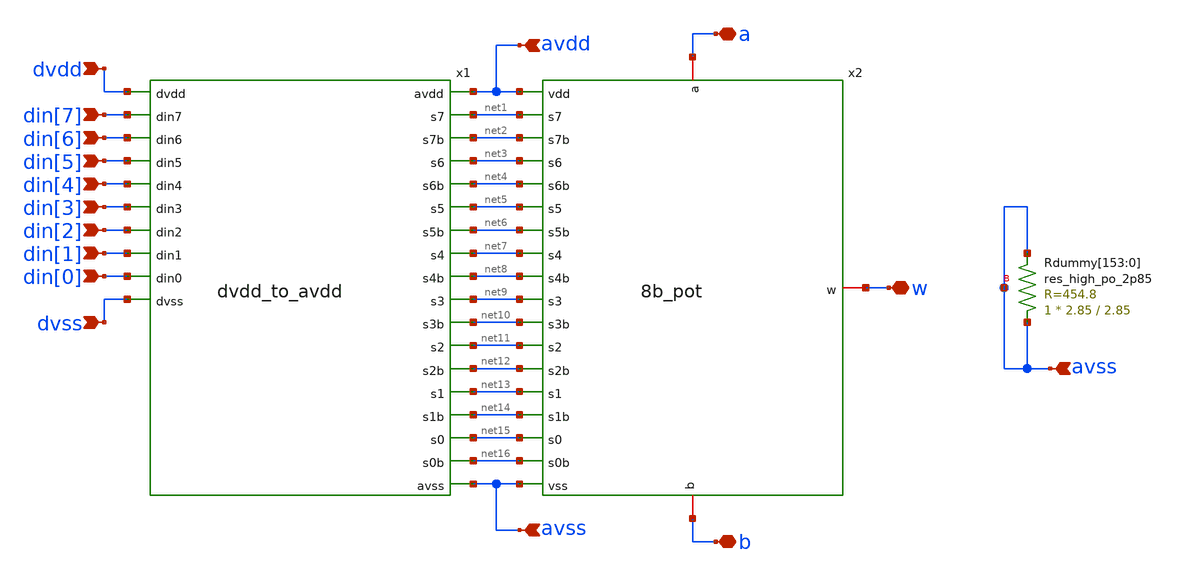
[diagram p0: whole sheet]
** sch_path: xschem/sky130_di_ip__rheostat_8bit.sch
**.subckt sky130_di_ip__rheostat_8bit avdd dvdd dvss avss b w a din[0] din[1] din[2] din[3] din[4]
*+ din[5] din[6] din[7] avss
*.ipin avdd
*.ipin dvdd
*.ipin dvss
*.ipin avss
*.iopin b
*.iopin w
*.iopin a
*.ipin din[0]
*.ipin din[1]
*.ipin din[2]
*.ipin din[3]
*.ipin din[4]
*.ipin din[5]
*.ipin din[6]
*.ipin din[7]
*.ipin avss
x1 avdd dvdd net1 din[7] net2 net3 din[6] net4 net5 din[5] net6 net7 din[4] net8 net9 din[3] net10
+ net11 din[2] net12 net13 din[1] net14 net15 din[0] net16 dvss avss dvdd_to_avdd
x2 avdd a net1 net2 net3 net4 net5 net6 net7 net8 w net9 net10 net11 net12 net13 net14 net15 net16 b
+ avss 8b_pot
XRdummy[153] avss avss avss sky130_fd_pr__res_high_po_2p85 L=2.85 mult=1 m=1
XRdummy[152] avss avss avss sky130_fd_pr__res_high_po_2p85 L=2.85 mult=1 m=1
XRdummy[151] avss avss avss sky130_fd_pr__res_high_po_2p85 L=2.85 mult=1 m=1
XRdummy[150] avss avss avss sky130_fd_pr__res_high_po_2p85 L=2.85 mult=1 m=1
XRdummy[149] avss avss avss sky130_fd_pr__res_high_po_2p85 L=2.85 mult=1 m=1
XRdummy[148] avss avss avss sky130_fd_pr__res_high_po_2p85 L=2.85 mult=1 m=1
XRdummy[147] avss avss avss sky130_fd_pr__res_high_po_2p85 L=2.85 mult=1 m=1
XRdummy[146] avss avss avss sky130_fd_pr__res_high_po_2p85 L=2.85 mult=1 m=1
XRdummy[145] avss avss avss sky130_fd_pr__res_high_po_2p85 L=2.85 mult=1 m=1
XRdummy[144] avss avss avss sky130_fd_pr__res_high_po_2p85 L=2.85 mult=1 m=1
XRdummy[143] avss avss avss sky130_fd_pr__res_high_po_2p85 L=2.85 mult=1 m=1
XRdummy[142] avss avss avss sky130_fd_pr__res_high_po_2p85 L=2.85 mult=1 m=1
XRdummy[141] avss avss avss sky130_fd_pr__res_high_po_2p85 L=2.85 mult=1 m=1
XRdummy[140] avss avss avss sky130_fd_pr__res_high_po_2p85 L=2.85 mult=1 m=1
XRdummy[139] avss avss avss sky130_fd_pr__res_high_po_2p85 L=2.85 mult=1 m=1
XRdummy[138] avss avss avss sky130_fd_pr__res_high_po_2p85 L=2.85 mult=1 m=1
XRdummy[137] avss avss avss sky130_fd_pr__res_high_po_2p85 L=2.85 mult=1 m=1
XRdummy[136] avss avss avss sky130_fd_pr__res_high_po_2p85 L=2.85 mult=1 m=1
XRdummy[135] avss avss avss sky130_fd_pr__res_high_po_2p85 L=2.85 mult=1 m=1
XRdummy[134] avss avss avss sky130_fd_pr__res_high_po_2p85 L=2.85 mult=1 m=1
XRdummy[133] avss avss avss sky130_fd_pr__res_high_po_2p85 L=2.85 mult=1 m=1
XRdummy[132] avss avss avss sky130_fd_pr__res_high_po_2p85 L=2.85 mult=1 m=1
XRdummy[131] avss avss avss sky130_fd_pr__res_high_po_2p85 L=2.85 mult=1 m=1
XRdummy[130] avss avss avss sky130_fd_pr__res_high_po_2p85 L=2.85 mult=1 m=1
XRdummy[129] avss avss avss sky130_fd_pr__res_high_po_2p85 L=2.85 mult=1 m=1
XRdummy[128] avss avss avss sky130_fd_pr__res_high_po_2p85 L=2.85 mult=1 m=1
XRdummy[127] avss avss avss sky130_fd_pr__res_high_po_2p85 L=2.85 mult=1 m=1
XRdummy[126] avss avss avss sky130_fd_pr__res_high_po_2p85 L=2.85 mult=1 m=1
XRdummy[125] avss avss avss sky130_fd_pr__res_high_po_2p85 L=2.85 mult=1 m=1
XRdummy[124] avss avss avss sky130_fd_pr__res_high_po_2p85 L=2.85 mult=1 m=1
XRdummy[123] avss avss avss sky130_fd_pr__res_high_po_2p85 L=2.85 mult=1 m=1
XRdummy[122] avss avss avss sky130_fd_pr__res_high_po_2p85 L=2.85 mult=1 m=1
XRdummy[121] avss avss avss sky130_fd_pr__res_high_po_2p85 L=2.85 mult=1 m=1
XRdummy[120] avss avss avss sky130_fd_pr__res_high_po_2p85 L=2.85 mult=1 m=1
XRdummy[119] avss avss avss sky130_fd_pr__res_high_po_2p85 L=2.85 mult=1 m=1
XRdummy[118] avss avss avss sky130_fd_pr__res_high_po_2p85 L=2.85 mult=1 m=1
XRdummy[117] avss avss avss sky130_fd_pr__res_high_po_2p85 L=2.85 mult=1 m=1
XRdummy[116] avss avss avss sky130_fd_pr__res_high_po_2p85 L=2.85 mult=1 m=1
XRdummy[115] avss avss avss sky130_fd_pr__res_high_po_2p85 L=2.85 mult=1 m=1
XRdummy[114] avss avss avss sky130_fd_pr__res_high_po_2p85 L=2.85 mult=1 m=1
XRdummy[113] avss avss avss sky130_fd_pr__res_high_po_2p85 L=2.85 mult=1 m=1
XRdummy[112] avss avss avss sky130_fd_pr__res_high_po_2p85 L=2.85 mult=1 m=1
XRdummy[111] avss avss avss sky130_fd_pr__res_high_po_2p85 L=2.85 mult=1 m=1
XRdummy[110] avss avss avss sky130_fd_pr__res_high_po_2p85 L=2.85 mult=1 m=1
XRdummy[109] avss avss avss sky130_fd_pr__res_high_po_2p85 L=2.85 mult=1 m=1
XRdummy[108] avss avss avss sky130_fd_pr__res_high_po_2p85 L=2.85 mult=1 m=1
XRdummy[107] avss avss avss sky130_fd_pr__res_high_po_2p85 L=2.85 mult=1 m=1
XRdummy[106] avss avss avss sky130_fd_pr__res_high_po_2p85 L=2.85 mult=1 m=1
XRdummy[105] avss avss avss sky130_fd_pr__res_high_po_2p85 L=2.85 mult=1 m=1
XRdummy[104] avss avss avss sky130_fd_pr__res_high_po_2p85 L=2.85 mult=1 m=1
XRdummy[103] avss avss avss sky130_fd_pr__res_high_po_2p85 L=2.85 mult=1 m=1
XRdummy[102] avss avss avss sky130_fd_pr__res_high_po_2p85 L=2.85 mult=1 m=1
XRdummy[101] avss avss avss sky130_fd_pr__res_high_po_2p85 L=2.85 mult=1 m=1
XRdummy[100] avss avss avss sky130_fd_pr__res_high_po_2p85 L=2.85 mult=1 m=1
XRdummy[99] avss avss avss sky130_fd_pr__res_high_po_2p85 L=2.85 mult=1 m=1
XRdummy[98] avss avss avss sky130_fd_pr__res_high_po_2p85 L=2.85 mult=1 m=1
XRdummy[97] avss avss avss sky130_fd_pr__res_high_po_2p85 L=2.85 mult=1 m=1
XRdummy[96] avss avss avss sky130_fd_pr__res_high_po_2p85 L=2.85 mult=1 m=1
XRdummy[95] avss avss avss sky130_fd_pr__res_high_po_2p85 L=2.85 mult=1 m=1
XRdummy[94] avss avss avss sky130_fd_pr__res_high_po_2p85 L=2.85 mult=1 m=1
XRdummy[93] avss avss avss sky130_fd_pr__res_high_po_2p85 L=2.85 mult=1 m=1
XRdummy[92] avss avss avss sky130_fd_pr__res_high_po_2p85 L=2.85 mult=1 m=1
XRdummy[91] avss avss avss sky130_fd_pr__res_high_po_2p85 L=2.85 mult=1 m=1
XRdummy[90] avss avss avss sky130_fd_pr__res_high_po_2p85 L=2.85 mult=1 m=1
XRdummy[89] avss avss avss sky130_fd_pr__res_high_po_2p85 L=2.85 mult=1 m=1
XRdummy[88] avss avss avss sky130_fd_pr__res_high_po_2p85 L=2.85 mult=1 m=1
XRdummy[87] avss avss avss sky130_fd_pr__res_high_po_2p85 L=2.85 mult=1 m=1
XRdummy[86] avss avss avss sky130_fd_pr__res_high_po_2p85 L=2.85 mult=1 m=1
XRdummy[85] avss avss avss sky130_fd_pr__res_high_po_2p85 L=2.85 mult=1 m=1
XRdummy[84] avss avss avss sky130_fd_pr__res_high_po_2p85 L=2.85 mult=1 m=1
XRdummy[83] avss avss avss sky130_fd_pr__res_high_po_2p85 L=2.85 mult=1 m=1
XRdummy[82] avss avss avss sky130_fd_pr__res_high_po_2p85 L=2.85 mult=1 m=1
XRdummy[81] avss avss avss sky130_fd_pr__res_high_po_2p85 L=2.85 mult=1 m=1
XRdummy[80] avss avss avss sky130_fd_pr__res_high_po_2p85 L=2.85 mult=1 m=1
XRdummy[79] avss avss avss sky130_fd_pr__res_high_po_2p85 L=2.85 mult=1 m=1
XRdummy[78] avss avss avss sky130_fd_pr__res_high_po_2p85 L=2.85 mult=1 m=1
XRdummy[77] avss avss avss sky130_fd_pr__res_high_po_2p85 L=2.85 mult=1 m=1
XRdummy[76] avss avss avss sky130_fd_pr__res_high_po_2p85 L=2.85 mult=1 m=1
XRdummy[75] avss avss avss sky130_fd_pr__res_high_po_2p85 L=2.85 mult=1 m=1
XRdummy[74] avss avss avss sky130_fd_pr__res_high_po_2p85 L=2.85 mult=1 m=1
XRdummy[73] avss avss avss sky130_fd_pr__res_high_po_2p85 L=2.85 mult=1 m=1
XRdummy[72] avss avss avss sky130_fd_pr__res_high_po_2p85 L=2.85 mult=1 m=1
XRdummy[71] avss avss avss sky130_fd_pr__res_high_po_2p85 L=2.85 mult=1 m=1
XRdummy[70] avss avss avss sky130_fd_pr__res_high_po_2p85 L=2.85 mult=1 m=1
XRdummy[69] avss avss avss sky130_fd_pr__res_high_po_2p85 L=2.85 mult=1 m=1
XRdummy[68] avss avss avss sky130_fd_pr__res_high_po_2p85 L=2.85 mult=1 m=1
XRdummy[67] avss avss avss sky130_fd_pr__res_high_po_2p85 L=2.85 mult=1 m=1
XRdummy[66] avss avss avss sky130_fd_pr__res_high_po_2p85 L=2.85 mult=1 m=1
XRdummy[65] avss avss avss sky130_fd_pr__res_high_po_2p85 L=2.85 mult=1 m=1
XRdummy[64] avss avss avss sky130_fd_pr__res_high_po_2p85 L=2.85 mult=1 m=1
XRdummy[63] avss avss avss sky130_fd_pr__res_high_po_2p85 L=2.85 mult=1 m=1
XRdummy[62] avss avss avss sky130_fd_pr__res_high_po_2p85 L=2.85 mult=1 m=1
XRdummy[61] avss avss avss sky130_fd_pr__res_high_po_2p85 L=2.85 mult=1 m=1
XRdummy[60] avss avss avss sky130_fd_pr__res_high_po_2p85 L=2.85 mult=1 m=1
XRdummy[59] avss avss avss sky130_fd_pr__res_high_po_2p85 L=2.85 mult=1 m=1
XRdummy[58] avss avss avss sky130_fd_pr__res_high_po_2p85 L=2.85 mult=1 m=1
XRdummy[57] avss avss avss sky130_fd_pr__res_high_po_2p85 L=2.85 mult=1 m=1
XRdummy[56] avss avss avss sky130_fd_pr__res_high_po_2p85 L=2.85 mult=1 m=1
XRdummy[55] avss avss avss sky130_fd_pr__res_high_po_2p85 L=2.85 mult=1 m=1
XRdummy[54] avss avss avss sky130_fd_pr__res_high_po_2p85 L=2.85 mult=1 m=1
XRdummy[53] avss avss avss sky130_fd_pr__res_high_po_2p85 L=2.85 mult=1 m=1
XRdummy[52] avss avss avss sky130_fd_pr__res_high_po_2p85 L=2.85 mult=1 m=1
XRdummy[51] avss avss avss sky130_fd_pr__res_high_po_2p85 L=2.85 mult=1 m=1
XRdummy[50] avss avss avss sky130_fd_pr__res_high_po_2p85 L=2.85 mult=1 m=1
XRdummy[49] avss avss avss sky130_fd_pr__res_high_po_2p85 L=2.85 mult=1 m=1
XRdummy[48] avss avss avss sky130_fd_pr__res_high_po_2p85 L=2.85 mult=1 m=1
XRdummy[47] avss avss avss sky130_fd_pr__res_high_po_2p85 L=2.85 mult=1 m=1
XRdummy[46] avss avss avss sky130_fd_pr__res_high_po_2p85 L=2.85 mult=1 m=1
XRdummy[45] avss avss avss sky130_fd_pr__res_high_po_2p85 L=2.85 mult=1 m=1
XRdummy[44] avss avss avss sky130_fd_pr__res_high_po_2p85 L=2.85 mult=1 m=1
XRdummy[43] avss avss avss sky130_fd_pr__res_high_po_2p85 L=2.85 mult=1 m=1
XRdummy[42] avss avss avss sky130_fd_pr__res_high_po_2p85 L=2.85 mult=1 m=1
XRdummy[41] avss avss avss sky130_fd_pr__res_high_po_2p85 L=2.85 mult=1 m=1
XRdummy[40] avss avss avss sky130_fd_pr__res_high_po_2p85 L=2.85 mult=1 m=1
XRdummy[39] avss avss avss sky130_fd_pr__res_high_po_2p85 L=2.85 mult=1 m=1
XRdummy[38] avss avss avss sky130_fd_pr__res_high_po_2p85 L=2.85 mult=1 m=1
XRdummy[37] avss avss avss sky130_fd_pr__res_high_po_2p85 L=2.85 mult=1 m=1
XRdummy[36] avss avss avss sky130_fd_pr__res_high_po_2p85 L=2.85 mult=1 m=1
XRdummy[35] avss avss avss sky130_fd_pr__res_high_po_2p85 L=2.85 mult=1 m=1
XRdummy[34] avss avss avss sky130_fd_pr__res_high_po_2p85 L=2.85 mult=1 m=1
XRdummy[33] avss avss avss sky130_fd_pr__res_high_po_2p85 L=2.85 mult=1 m=1
XRdummy[32] avss avss avss sky130_fd_pr__res_high_po_2p85 L=2.85 mult=1 m=1
XRdummy[31] avss avss avss sky130_fd_pr__res_high_po_2p85 L=2.85 mult=1 m=1
XRdummy[30] avss avss avss sky130_fd_pr__res_high_po_2p85 L=2.85 mult=1 m=1
XRdummy[29] avss avss avss sky130_fd_pr__res_high_po_2p85 L=2.85 mult=1 m=1
XRdummy[28] avss avss avss sky130_fd_pr__res_high_po_2p85 L=2.85 mult=1 m=1
XRdummy[27] avss avss avss sky130_fd_pr__res_high_po_2p85 L=2.85 mult=1 m=1
XRdummy[26] avss avss avss sky130_fd_pr__res_high_po_2p85 L=2.85 mult=1 m=1
XRdummy[25] avss avss avss sky130_fd_pr__res_high_po_2p85 L=2.85 mult=1 m=1
XRdummy[24] avss avss avss sky130_fd_pr__res_high_po_2p85 L=2.85 mult=1 m=1
XRdummy[23] avss avss avss sky130_fd_pr__res_high_po_2p85 L=2.85 mult=1 m=1
XRdummy[22] avss avss avss sky130_fd_pr__res_high_po_2p85 L=2.85 mult=1 m=1
XRdummy[21] avss avss avss sky130_fd_pr__res_high_po_2p85 L=2.85 mult=1 m=1
XRdummy[20] avss avss avss sky130_fd_pr__res_high_po_2p85 L=2.85 mult=1 m=1
XRdummy[19] avss avss avss sky130_fd_pr__res_high_po_2p85 L=2.85 mult=1 m=1
XRdummy[18] avss avss avss sky130_fd_pr__res_high_po_2p85 L=2.85 mult=1 m=1
XRdummy[17] avss avss avss sky130_fd_pr__res_high_po_2p85 L=2.85 mult=1 m=1
XRdummy[16] avss avss avss sky130_fd_pr__res_high_po_2p85 L=2.85 mult=1 m=1
XRdummy[15] avss avss avss sky130_fd_pr__res_high_po_2p85 L=2.85 mult=1 m=1
XRdummy[14] avss avss avss sky130_fd_pr__res_high_po_2p85 L=2.85 mult=1 m=1
XRdummy[13] avss avss avss sky130_fd_pr__res_high_po_2p85 L=2.85 mult=1 m=1
XRdummy[12] avss avss avss sky130_fd_pr__res_high_po_2p85 L=2.85 mult=1 m=1
XRdummy[11] avss avss avss sky130_fd_pr__res_high_po_2p85 L=2.85 mult=1 m=1
XRdummy[10] avss avss avss sky130_fd_pr__res_high_po_2p85 L=2.85 mult=1 m=1
XRdummy[9] avss avss avss sky130_fd_pr__res_high_po_2p85 L=2.85 mult=1 m=1
XRdummy[8] avss avss avss sky130_fd_pr__res_high_po_2p85 L=2.85 mult=1 m=1
XRdummy[7] avss avss avss sky130_fd_pr__res_high_po_2p85 L=2.85 mult=1 m=1
XRdummy[6] avss avss avss sky130_fd_pr__res_high_po_2p85 L=2.85 mult=1 m=1
XRdummy[5] avss avss avss sky130_fd_pr__res_high_po_2p85 L=2.85 mult=1 m=1
XRdummy[4] avss avss avss sky130_fd_pr__res_high_po_2p85 L=2.85 mult=1 m=1
XRdummy[3] avss avss avss sky130_fd_pr__res_high_po_2p85 L=2.85 mult=1 m=1
XRdummy[2] avss avss avss sky130_fd_pr__res_high_po_2p85 L=2.85 mult=1 m=1
XRdummy[1] avss avss avss sky130_fd_pr__res_high_po_2p85 L=2.85 mult=1 m=1
XRdummy[0] avss avss avss sky130_fd_pr__res_high_po_2p85 L=2.85 mult=1 m=1
**.ends
.end
